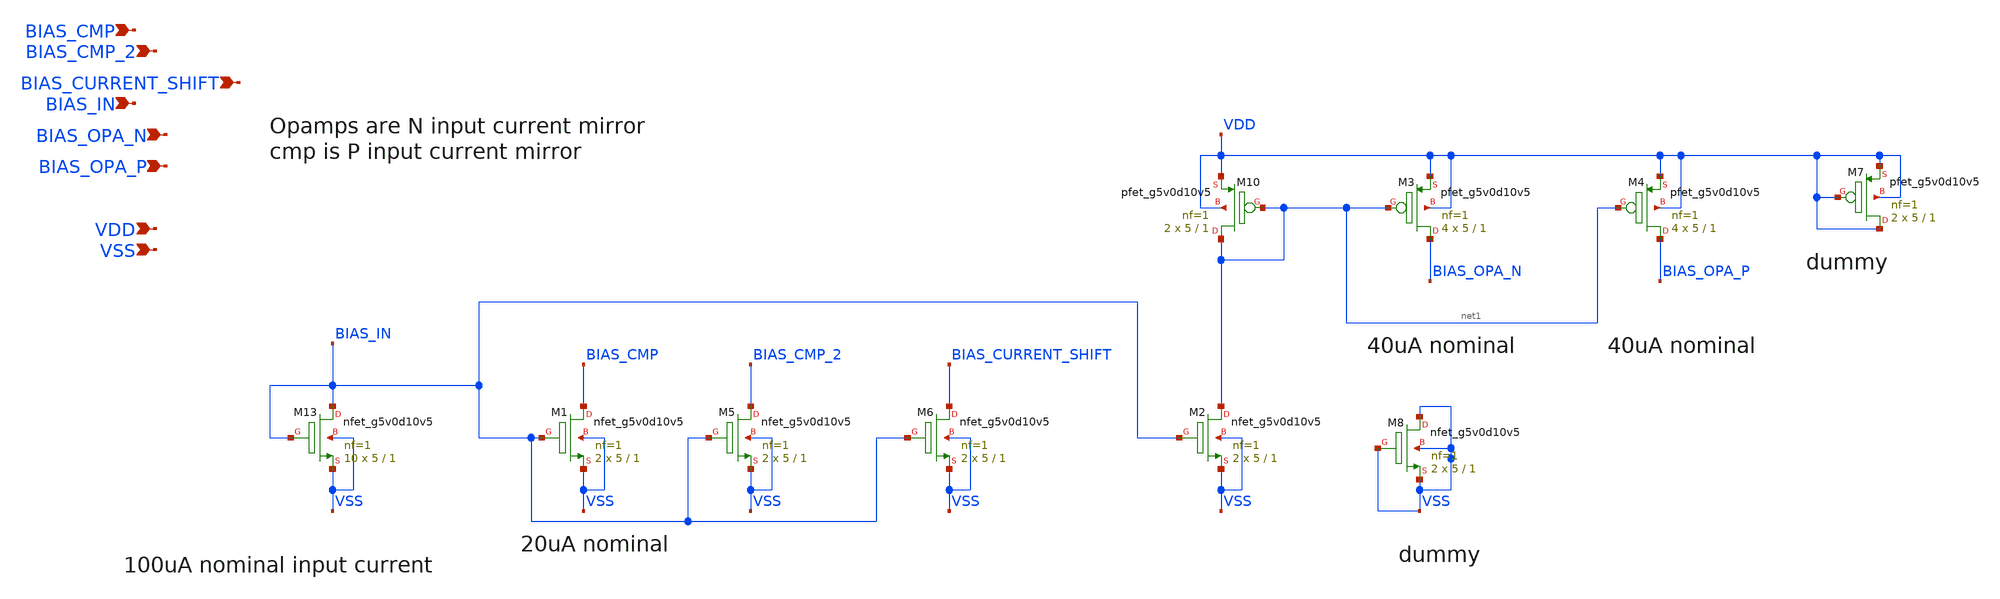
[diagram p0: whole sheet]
** sch_path: images/iic-osic-tools/addons/examples/open-pmic/design/bias-circuit/bias_distribution.sch
**.subckt bias_distribution BIAS_CMP BIAS_CMP_2 BIAS_CURRENT_SHIFT BIAS_IN BIAS_OPA_N BIAS_OPA_P VDD
*+ VSS
*.ipin BIAS_CMP
*.ipin BIAS_CMP_2
*.ipin BIAS_CURRENT_SHIFT
*.ipin BIAS_IN
*.ipin BIAS_OPA_N
*.ipin BIAS_OPA_P
*.ipin VDD
*.ipin VSS
XM10 net1 net1 VDD VDD sky130_fd_pr__pfet_g5v0d10v5 L=1 W=5 nf=1 ad='int((nf+1)/2) * W/nf * 0.29' as='int((nf+2)/2) * W/nf * 0.29'
+ pd='2*int((nf+1)/2) * (W/nf + 0.29)' ps='2*int((nf+2)/2) * (W/nf + 0.29)' nrd='0.29 / W' nrs='0.29 / W'
+ sa=0 sb=0 sd=0 mult=2 m=2
XM1 BIAS_CMP BIAS_IN VSS VSS sky130_fd_pr__nfet_g5v0d10v5 L=1 W=5 nf=1 ad='int((nf+1)/2) * W/nf * 0.29'
+ as='int((nf+2)/2) * W/nf * 0.29' pd='2*int((nf+1)/2) * (W/nf + 0.29)' ps='2*int((nf+2)/2) * (W/nf + 0.29)'
+ nrd='0.29 / W' nrs='0.29 / W' sa=0 sb=0 sd=0 mult=2 m=2
XM2 net1 BIAS_IN VSS VSS sky130_fd_pr__nfet_g5v0d10v5 L=1 W=5 nf=1 ad='int((nf+1)/2) * W/nf * 0.29' as='int((nf+2)/2) * W/nf * 0.29'
+ pd='2*int((nf+1)/2) * (W/nf + 0.29)' ps='2*int((nf+2)/2) * (W/nf + 0.29)' nrd='0.29 / W' nrs='0.29 / W'
+ sa=0 sb=0 sd=0 mult=2 m=2
XM3 BIAS_OPA_N net1 VDD VDD sky130_fd_pr__pfet_g5v0d10v5 L=1 W=5 nf=1 ad='int((nf+1)/2) * W/nf * 0.29'
+ as='int((nf+2)/2) * W/nf * 0.29' pd='2*int((nf+1)/2) * (W/nf + 0.29)' ps='2*int((nf+2)/2) * (W/nf + 0.29)'
+ nrd='0.29 / W' nrs='0.29 / W' sa=0 sb=0 sd=0 mult=4 m=4
XM4 BIAS_OPA_P net1 VDD VDD sky130_fd_pr__pfet_g5v0d10v5 L=1 W=5 nf=1 ad='int((nf+1)/2) * W/nf * 0.29'
+ as='int((nf+2)/2) * W/nf * 0.29' pd='2*int((nf+1)/2) * (W/nf + 0.29)' ps='2*int((nf+2)/2) * (W/nf + 0.29)'
+ nrd='0.29 / W' nrs='0.29 / W' sa=0 sb=0 sd=0 mult=4 m=4
XM5 BIAS_CMP_2 BIAS_IN VSS VSS sky130_fd_pr__nfet_g5v0d10v5 L=1 W=5 nf=1 ad='int((nf+1)/2) * W/nf * 0.29'
+ as='int((nf+2)/2) * W/nf * 0.29' pd='2*int((nf+1)/2) * (W/nf + 0.29)' ps='2*int((nf+2)/2) * (W/nf + 0.29)'
+ nrd='0.29 / W' nrs='0.29 / W' sa=0 sb=0 sd=0 mult=2 m=2
XM13 BIAS_IN BIAS_IN VSS VSS sky130_fd_pr__nfet_g5v0d10v5 L=1 W=5 nf=1 ad='int((nf+1)/2) * W/nf * 0.29'
+ as='int((nf+2)/2) * W/nf * 0.29' pd='2*int((nf+1)/2) * (W/nf + 0.29)' ps='2*int((nf+2)/2) * (W/nf + 0.29)'
+ nrd='0.29 / W' nrs='0.29 / W' sa=0 sb=0 sd=0 mult=10 m=10
XM6 BIAS_CURRENT_SHIFT BIAS_IN VSS VSS sky130_fd_pr__nfet_g5v0d10v5 L=1 W=5 nf=1 ad='int((nf+1)/2) * W/nf * 0.29'
+ as='int((nf+2)/2) * W/nf * 0.29' pd='2*int((nf+1)/2) * (W/nf + 0.29)' ps='2*int((nf+2)/2) * (W/nf + 0.29)'
+ nrd='0.29 / W' nrs='0.29 / W' sa=0 sb=0 sd=0 mult=2 m=2
XM7 VDD VDD VDD VDD sky130_fd_pr__pfet_g5v0d10v5 L=1 W=5 nf=1 ad='int((nf+1)/2) * W/nf * 0.29' as='int((nf+2)/2) * W/nf * 0.29'
+ pd='2*int((nf+1)/2) * (W/nf + 0.29)' ps='2*int((nf+2)/2) * (W/nf + 0.29)' nrd='0.29 / W' nrs='0.29 / W'
+ sa=0 sb=0 sd=0 mult=2 m=2
XM8 VSS VSS VSS VSS sky130_fd_pr__nfet_g5v0d10v5 L=1 W=5 nf=1 ad='int((nf+1)/2) * W/nf * 0.29' as='int((nf+2)/2) * W/nf * 0.29'
+ pd='2*int((nf+1)/2) * (W/nf + 0.29)' ps='2*int((nf+2)/2) * (W/nf + 0.29)' nrd='0.29 / W' nrs='0.29 / W'
+ sa=0 sb=0 sd=0 mult=2 m=2
**.ends
.end
